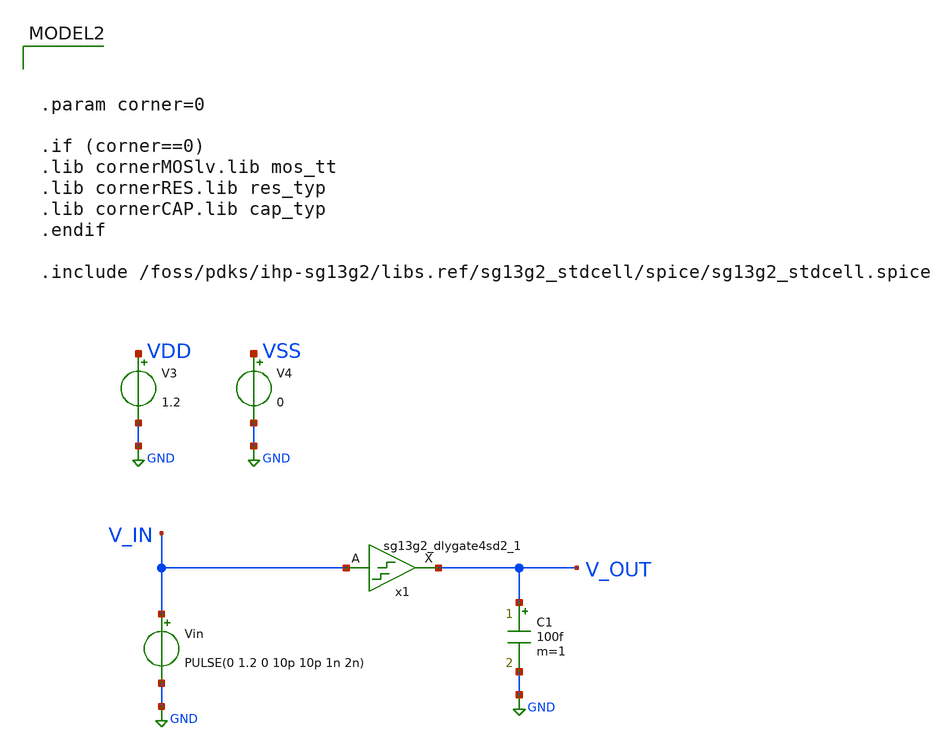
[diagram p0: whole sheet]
** sch_path: others/tb_std_delay.sch
* IHP-GmbH/IHP-Open-PDK/ihp-sg13g2/libs.tech/xschem/sg13g2_stdcells/sg13g2_dlygate4sd2_1.sch:
* Copyright 2023 IHP PDK Authors
* Licensed under the Apache License, Version 2.0 (the "License");
**.subckt tb_std_delay
C1 V_OUT GND 100f m=1
Vin V_IN GND PULSE(0 1.2 0 10p 10p 1n 2n)
x1 V_OUT V_IN VDD VSS sg13g2_dlygate4sd2_1
V3 VDD GND 1.2
V4 VSS GND 0
**** begin user architecture code


.control
* ---- settings you tweak ----
   * ---- user settings ----
  let vlow  = 0
  let vhigh = 1.2
  let v50   = vlow + 0.5*(vhigh - vlow)

  let start_edge = 5     ; skip early edges (settling)
  let N = 50             ; number of phase samples

  tran 1p 200n

  * ---- allocate vectors ----
  let tvec   = vector(N)
  let phivec = vector(N)

  let k = 0
  let i = start_edge

  while k < N
    * crossing times
    meas tran tin      WHEN v(v_in)=v50  RISE=i
    meas tran tout     WHEN v(v_out)=v50 RISE=i
    meas tran tin_next WHEN v(v_in)=v50  RISE=(i+1)

    * delay + period
    let dt = tout - tin
    let T  = tin_next - tin

    * phase in degrees (per-cycle)
    let phi = 360*dt/T

    * store sample at time = tin
    let tvec[k]   = tin
    let phivec[k] = phi

    let k = k + 1
    let i = i + 1
  end

  * plot phase vs time (one point per cycle)
  plot phivec vs tvec
  plot v(V_IN) v(V_OUT)
.endc




.param corner=0

.if (corner==0)
.lib cornerMOSlv.lib mos_tt
.lib cornerRES.lib res_typ
.lib cornerCAP.lib cap_typ
.endif

.include /foss/pdks/ihp-sg13g2/libs.ref/sg13g2_stdcell/spice/sg13g2_stdcell.spice
**** end user architecture code
**.ends

* expanding   symbol:  sg13g2_stdcells/sg13g2_dlygate4sd2_1.sym # of pins=2
** sym_path: sg13g2_stdcells/sg13g2_dlygate4sd2_1.sym
** sch_path: sg13g2_stdcells/sg13g2_dlygate4sd2_1.sch
.subckt sg13g2_dlygate4sd2_1 X A VDD VSS
*.ipin A
*.opin X
*.iopin VDD
*.iopin VSS
XM1 net2 A VSS VSS sg13_lv_nmos w=420.00n l=130.00n ng=1 m=1 mm_ok=1
XM2 net1 net2 VSS VSS sg13_lv_nmos w=420.00n l=180.00n ng=1 m=1 mm_ok=1
XM3 net3 net1 VSS VSS sg13_lv_nmos w=420.00n l=180.00n ng=1 m=1 mm_ok=1
XM4 X net3 VSS VSS sg13_lv_nmos w=740.00n l=130.00n ng=1 m=1 mm_ok=1
XM5 net2 A VDD VDD sg13_lv_pmos w=420.00n l=130.00n ng=1 m=1 mm_ok=1
XM6 net1 net2 VDD VDD sg13_lv_pmos w=1.000u l=250.00n ng=1 m=1 mm_ok=1
XM7 net3 net1 VDD VDD sg13_lv_pmos w=1.000u l=250.00n ng=1 m=1 mm_ok=1
XM8 X net3 VDD VDD sg13_lv_pmos w=1.12u l=130.00n ng=1 m=1 mm_ok=1
.ends

.GLOBAL GND
.end
